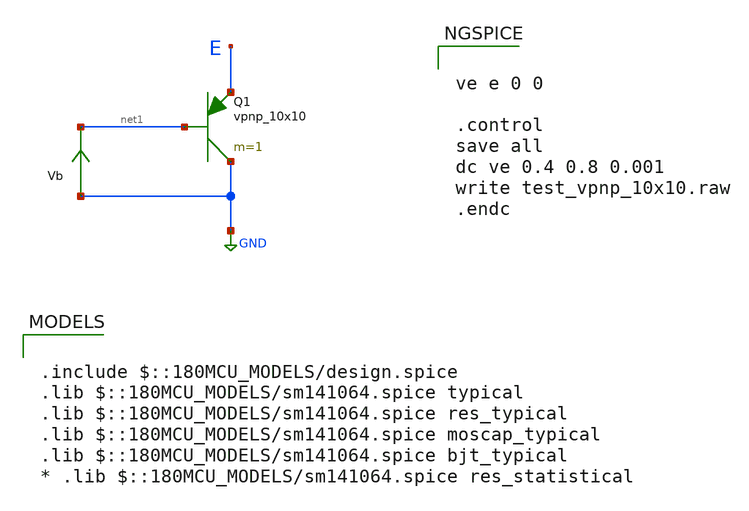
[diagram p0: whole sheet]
** sch_path: cells/xschem/tests/test_vpnp_10x10.sch
* Copyright 2022 GlobalFoundries PDK Authors
* Licensed under the Apache License, Version 2.0 (the "License");
* you may not use this file except in compliance with the License.
* You may obtain a copy of the License at
* https://www.apache.org/licenses/LICENSE-2.0
* Unless required by applicable law or agreed to in writing, software
* distributed under the License is distributed on an "AS IS" BASIS,
* WITHOUT WARRANTIES OR CONDITIONS OF ANY KIND, either express or implied.
* See the License for the specific language governing permissions and
* limitations under the License.
**.subckt test_vpnp_10x10
XQ1 GND net1 E vpnp_10x10 m=1
Vb GND net1 0
.save i(vb)
**** begin user architecture code

.include $::180MCU_MODELS/design.spice
.lib $::180MCU_MODELS/sm141064.spice typical
.lib $::180MCU_MODELS/sm141064.spice res_typical
.lib $::180MCU_MODELS/sm141064.spice moscap_typical
.lib $::180MCU_MODELS/sm141064.spice bjt_typical
* .lib $::180MCU_MODELS/sm141064.spice res_statistical



ve e 0 0

.control
save all
dc ve 0.4 0.8 0.001
write test_vpnp_10x10.raw
.endc


**** end user architecture code
**.ends
.GLOBAL GND
.end
